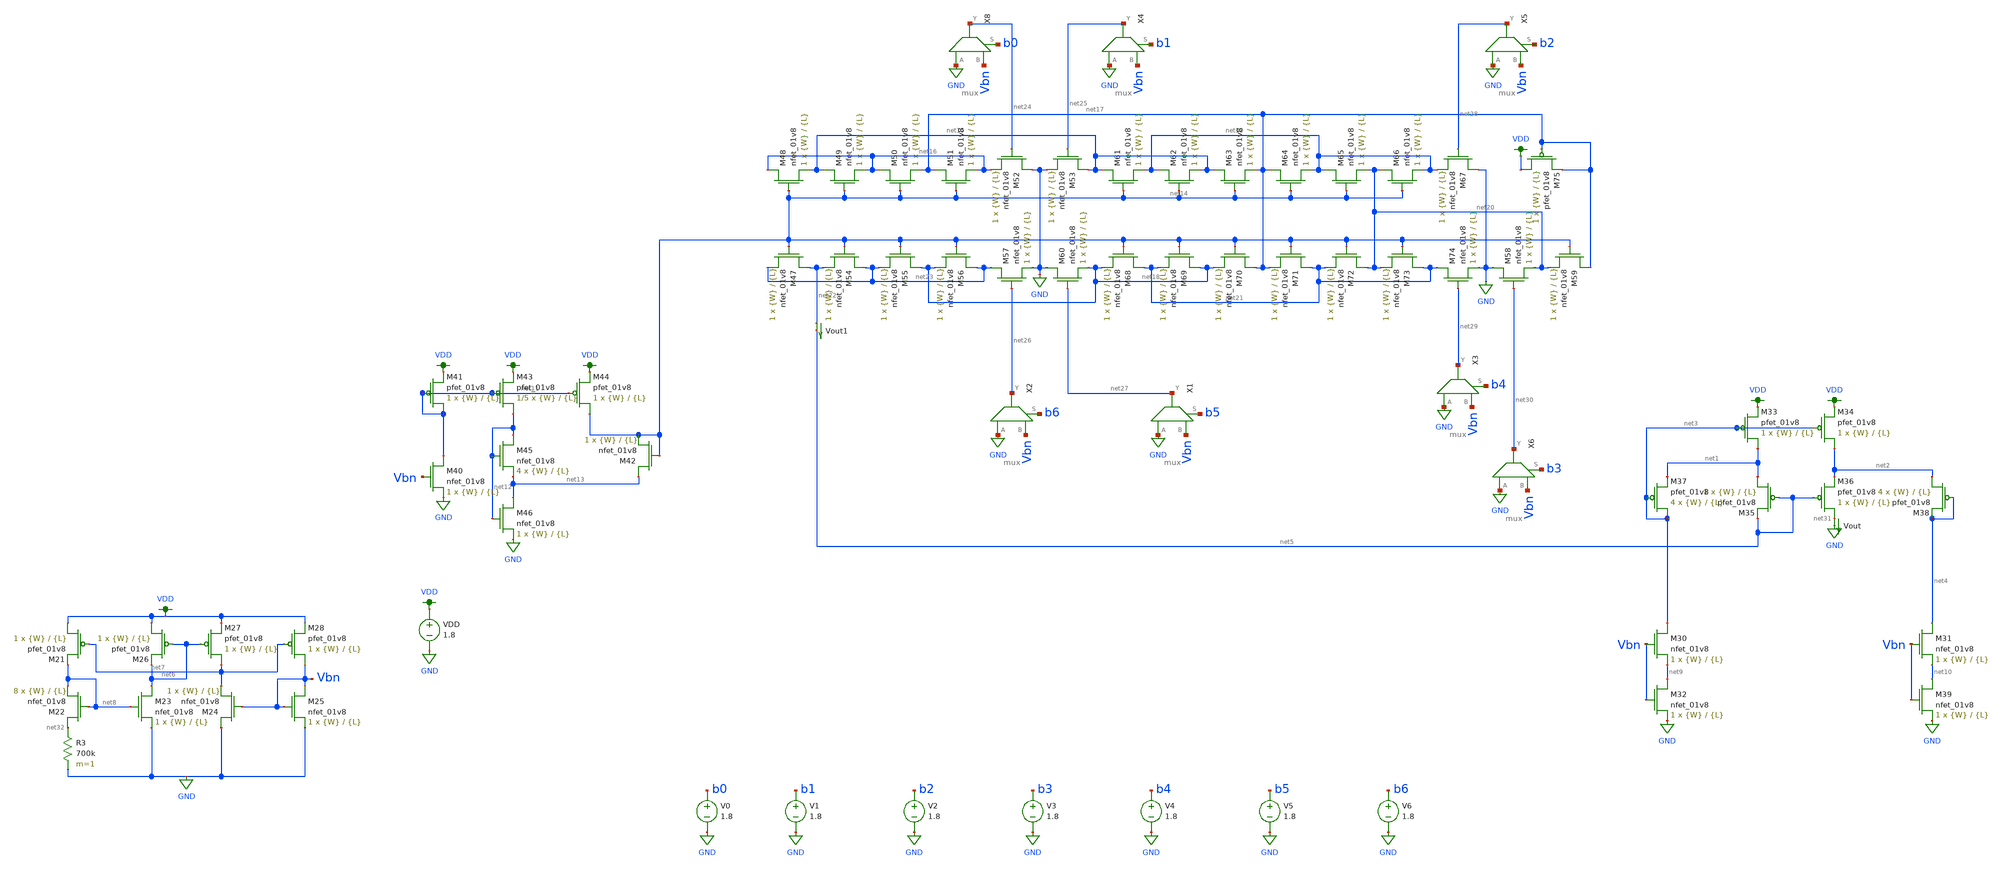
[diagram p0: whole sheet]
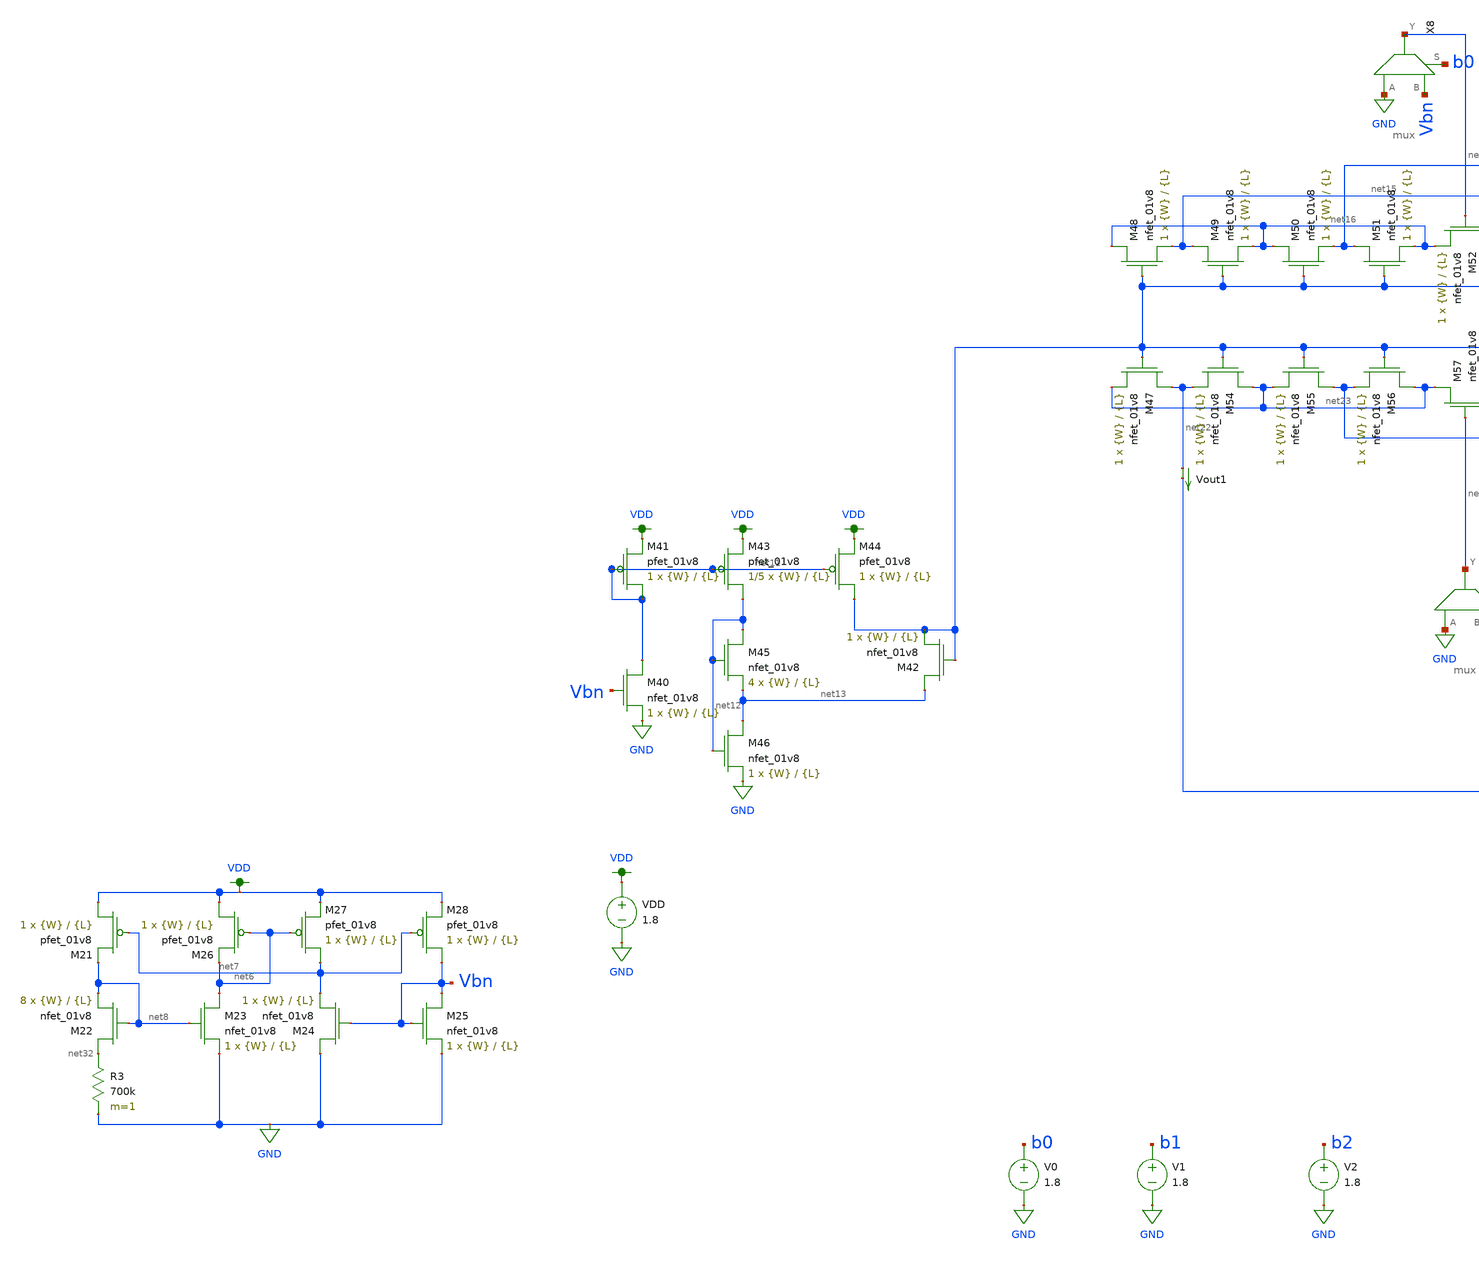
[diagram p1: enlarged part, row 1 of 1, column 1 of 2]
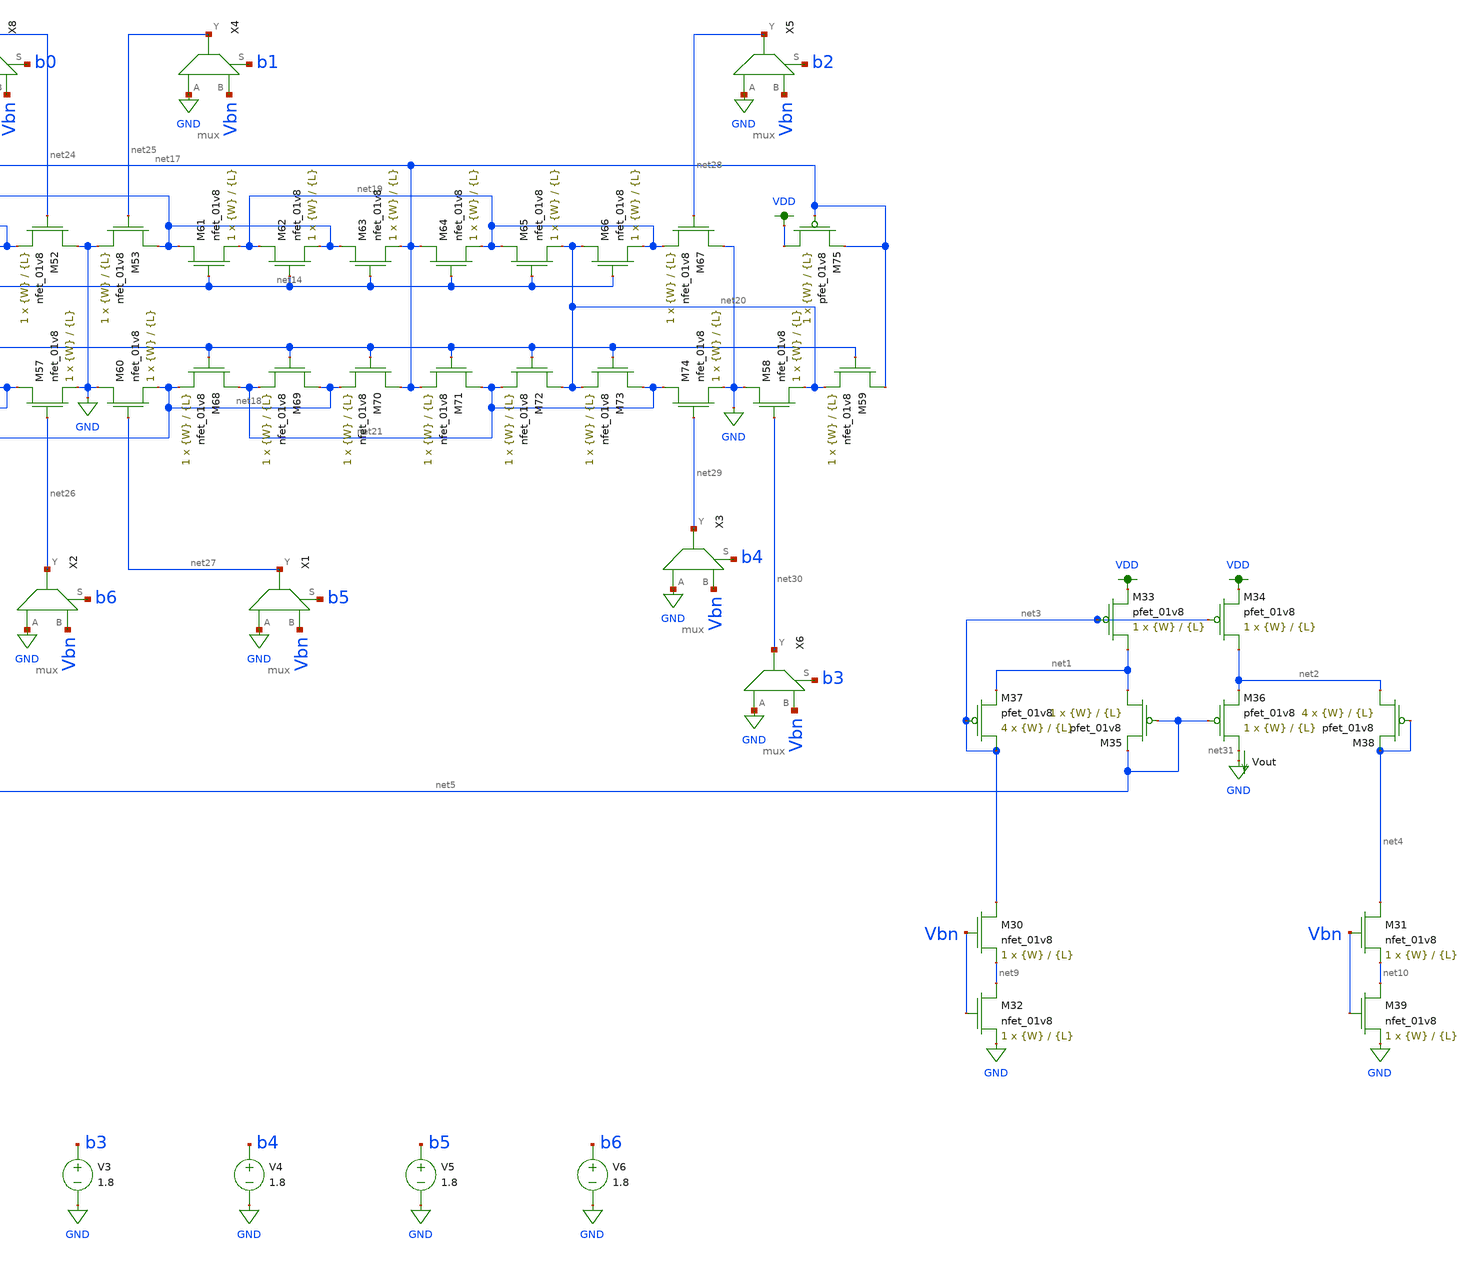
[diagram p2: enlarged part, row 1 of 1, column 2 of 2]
** sch_path: dac/schematics/misc/dac_lds_kenta.sch
**.subckt dac_lds_kenta
V0 b0 GND 1.8
V1 b1 GND 1.8
V2 b2 GND 1.8
V3 b3 GND 1.8
V4 b4 GND 1.8
V5 b5 GND 1.8
V6 b6 GND 1.8
Vout net31 GND 0
.save i(vout)
VDD VDD GND 1.8
XM33 net1 net3 VDD VDD sky130_fd_pr__pfet_01v8 L={L} W={W} nf=1 ad='int((nf+1)/2) * W/nf * 0.29' as='int((nf+2)/2) * W/nf * 0.29'
+ pd='2*int((nf+1)/2) * (W/nf + 0.29)' ps='2*int((nf+2)/2) * (W/nf + 0.29)' nrd='0.29 / W' nrs='0.29 / W'
+ sa=0 sb=0 sd=0 mult=1 m=1
XM34 net2 net3 VDD VDD sky130_fd_pr__pfet_01v8 L={L} W={W} nf=1 ad='int((nf+1)/2) * W/nf * 0.29' as='int((nf+2)/2) * W/nf * 0.29'
+ pd='2*int((nf+1)/2) * (W/nf + 0.29)' ps='2*int((nf+2)/2) * (W/nf + 0.29)' nrd='0.29 / W' nrs='0.29 / W'
+ sa=0 sb=0 sd=0 mult=1 m=1
XM35 net1 net5 net5 VDD sky130_fd_pr__pfet_01v8 L={L} W={W} nf=1 ad='int((nf+1)/2) * W/nf * 0.29' as='int((nf+2)/2) * W/nf * 0.29'
+ pd='2*int((nf+1)/2) * (W/nf + 0.29)' ps='2*int((nf+2)/2) * (W/nf + 0.29)' nrd='0.29 / W' nrs='0.29 / W'
+ sa=0 sb=0 sd=0 mult=1 m=1
XM36 net31 net5 net2 VDD sky130_fd_pr__pfet_01v8 L={L} W={W} nf=1 ad='int((nf+1)/2) * W/nf * 0.29' as='int((nf+2)/2) * W/nf * 0.29'
+ pd='2*int((nf+1)/2) * (W/nf + 0.29)' ps='2*int((nf+2)/2) * (W/nf + 0.29)' nrd='0.29 / W' nrs='0.29 / W'
+ sa=0 sb=0 sd=0 mult=1 m=1
XM37 net3 net3 net1 VDD sky130_fd_pr__pfet_01v8 L={L} W={W} nf=1 ad='int((nf+1)/2) * W/nf * 0.29' as='int((nf+2)/2) * W/nf * 0.29'
+ pd='2*int((nf+1)/2) * (W/nf + 0.29)' ps='2*int((nf+2)/2) * (W/nf + 0.29)' nrd='0.29 / W' nrs='0.29 / W'
+ sa=0 sb=0 sd=0 mult=4 m=4
XM38 net2 net4 net4 VDD sky130_fd_pr__pfet_01v8 L={L} W={W} nf=1 ad='int((nf+1)/2) * W/nf * 0.29' as='int((nf+2)/2) * W/nf * 0.29'
+ pd='2*int((nf+1)/2) * (W/nf + 0.29)' ps='2*int((nf+2)/2) * (W/nf + 0.29)' nrd='0.29 / W' nrs='0.29 / W'
+ sa=0 sb=0 sd=0 mult=4 m=4
XM21 VDD net7 net8 VDD sky130_fd_pr__pfet_01v8 L={L} W={W} nf=1 ad='int((nf+1)/2) * W/nf * 0.29' as='int((nf+2)/2) * W/nf * 0.29'
+ pd='2*int((nf+1)/2) * (W/nf + 0.29)' ps='2*int((nf+2)/2) * (W/nf + 0.29)' nrd='0.29 / W' nrs='0.29 / W'
+ sa=0 sb=0 sd=0 mult=1 m=1
XM22 net32 net8 net8 GND sky130_fd_pr__nfet_01v8 L={L} W={W} nf=1 ad='int((nf+1)/2) * W/nf * 0.29' as='int((nf+2)/2) * W/nf * 0.29'
+ pd='2*int((nf+1)/2) * (W/nf + 0.29)' ps='2*int((nf+2)/2) * (W/nf + 0.29)' nrd='0.29 / W' nrs='0.29 / W'
+ sa=0 sb=0 sd=0 mult=8 m=8
R3 net32 GND 700k m=1
XM23 net6 net8 GND GND sky130_fd_pr__nfet_01v8 L={L} W={W} nf=1 ad='int((nf+1)/2) * W/nf * 0.29' as='int((nf+2)/2) * W/nf * 0.29'
+ pd='2*int((nf+1)/2) * (W/nf + 0.29)' ps='2*int((nf+2)/2) * (W/nf + 0.29)' nrd='0.29 / W' nrs='0.29 / W'
+ sa=0 sb=0 sd=0 mult=1 m=1
XM24 GND Vbn net7 GND sky130_fd_pr__nfet_01v8 L={L} W={W} nf=1 ad='int((nf+1)/2) * W/nf * 0.29' as='int((nf+2)/2) * W/nf * 0.29'
+ pd='2*int((nf+1)/2) * (W/nf + 0.29)' ps='2*int((nf+2)/2) * (W/nf + 0.29)' nrd='0.29 / W' nrs='0.29 / W'
+ sa=0 sb=0 sd=0 mult=1 m=1
XM25 Vbn Vbn GND GND sky130_fd_pr__nfet_01v8 L={L} W={W} nf=1 ad='int((nf+1)/2) * W/nf * 0.29' as='int((nf+2)/2) * W/nf * 0.29'
+ pd='2*int((nf+1)/2) * (W/nf + 0.29)' ps='2*int((nf+2)/2) * (W/nf + 0.29)' nrd='0.29 / W' nrs='0.29 / W'
+ sa=0 sb=0 sd=0 mult=1 m=1
XM26 VDD net6 net6 VDD sky130_fd_pr__pfet_01v8 L={L} W={W} nf=1 ad='int((nf+1)/2) * W/nf * 0.29' as='int((nf+2)/2) * W/nf * 0.29'
+ pd='2*int((nf+1)/2) * (W/nf + 0.29)' ps='2*int((nf+2)/2) * (W/nf + 0.29)' nrd='0.29 / W' nrs='0.29 / W'
+ sa=0 sb=0 sd=0 mult=1 m=1
XM27 net7 net6 VDD VDD sky130_fd_pr__pfet_01v8 L={L} W={W} nf=1 ad='int((nf+1)/2) * W/nf * 0.29' as='int((nf+2)/2) * W/nf * 0.29'
+ pd='2*int((nf+1)/2) * (W/nf + 0.29)' ps='2*int((nf+2)/2) * (W/nf + 0.29)' nrd='0.29 / W' nrs='0.29 / W'
+ sa=0 sb=0 sd=0 mult=1 m=1
XM28 Vbn net7 VDD VDD sky130_fd_pr__pfet_01v8 L={L} W={W} nf=1 ad='int((nf+1)/2) * W/nf * 0.29' as='int((nf+2)/2) * W/nf * 0.29'
+ pd='2*int((nf+1)/2) * (W/nf + 0.29)' ps='2*int((nf+2)/2) * (W/nf + 0.29)' nrd='0.29 / W' nrs='0.29 / W'
+ sa=0 sb=0 sd=0 mult=1 m=1
XM30 net3 Vbn net9 GND sky130_fd_pr__nfet_01v8 L={L} W={W} nf=1 ad='int((nf+1)/2) * W/nf * 0.29' as='int((nf+2)/2) * W/nf * 0.29'
+ pd='2*int((nf+1)/2) * (W/nf + 0.29)' ps='2*int((nf+2)/2) * (W/nf + 0.29)' nrd='0.29 / W' nrs='0.29 / W'
+ sa=0 sb=0 sd=0 mult=1 m=1
XM31 net4 Vbn net10 GND sky130_fd_pr__nfet_01v8 L={L} W={W} nf=1 ad='int((nf+1)/2) * W/nf * 0.29' as='int((nf+2)/2) * W/nf * 0.29'
+ pd='2*int((nf+1)/2) * (W/nf + 0.29)' ps='2*int((nf+2)/2) * (W/nf + 0.29)' nrd='0.29 / W' nrs='0.29 / W'
+ sa=0 sb=0 sd=0 mult=1 m=1
XM32 net9 Vbn GND GND sky130_fd_pr__nfet_01v8 L={L} W={W} nf=1 ad='int((nf+1)/2) * W/nf * 0.29' as='int((nf+2)/2) * W/nf * 0.29'
+ pd='2*int((nf+1)/2) * (W/nf + 0.29)' ps='2*int((nf+2)/2) * (W/nf + 0.29)' nrd='0.29 / W' nrs='0.29 / W'
+ sa=0 sb=0 sd=0 mult=1 m=1
XM39 net10 Vbn GND GND sky130_fd_pr__nfet_01v8 L={L} W={W} nf=1 ad='int((nf+1)/2) * W/nf * 0.29' as='int((nf+2)/2) * W/nf * 0.29'
+ pd='2*int((nf+1)/2) * (W/nf + 0.29)' ps='2*int((nf+2)/2) * (W/nf + 0.29)' nrd='0.29 / W' nrs='0.29 / W'
+ sa=0 sb=0 sd=0 mult=1 m=1
X8 GND Vbn net24 b0 mux
X4 GND Vbn net25 b1 mux
X5 GND Vbn net28 b2 mux
X6 GND Vbn net30 b3 mux
X3 GND Vbn net29 b4 mux
X1 GND Vbn net27 b5 mux
X2 GND Vbn net26 b6 mux
Vout1 net22 net5 0
.save i(vout1)
XM40 net11 Vbn GND GND sky130_fd_pr__nfet_01v8 L={L} W={W} nf=1 ad='int((nf+1)/2) * W/nf * 0.29' as='int((nf+2)/2) * W/nf * 0.29'
+ pd='2*int((nf+1)/2) * (W/nf + 0.29)' ps='2*int((nf+2)/2) * (W/nf + 0.29)' nrd='0.29 / W' nrs='0.29 / W'
+ sa=0 sb=0 sd=0 mult=1 m=1
XM41 net11 net11 VDD VDD sky130_fd_pr__pfet_01v8 L={L} W={W} nf=1 ad='int((nf+1)/2) * W/nf * 0.29' as='int((nf+2)/2) * W/nf * 0.29'
+ pd='2*int((nf+1)/2) * (W/nf + 0.29)' ps='2*int((nf+2)/2) * (W/nf + 0.29)' nrd='0.29 / W' nrs='0.29 / W'
+ sa=0 sb=0 sd=0 mult=1 m=1
XM42 net13 net14 net14 GND sky130_fd_pr__nfet_01v8 L={L} W={W} nf=1 ad='int((nf+1)/2) * W/nf * 0.29'
+ as='int((nf+2)/2) * W/nf * 0.29' pd='2*int((nf+1)/2) * (W/nf + 0.29)' ps='2*int((nf+2)/2) * (W/nf + 0.29)'
+ nrd='0.29 / W' nrs='0.29 / W' sa=0 sb=0 sd=0 mult=1 m=1
XM43 net12 net11 VDD VDD sky130_fd_pr__pfet_01v8 L={L} W={W} nf=1 ad='int((nf+1)/2) * W/nf * 0.29' as='int((nf+2)/2) * W/nf * 0.29'
+ pd='2*int((nf+1)/2) * (W/nf + 0.29)' ps='2*int((nf+2)/2) * (W/nf + 0.29)' nrd='0.29 / W' nrs='0.29 / W'
+ sa=0 sb=0 sd=0 mult=1/5 m=1/5
XM44 net14 net11 VDD VDD sky130_fd_pr__pfet_01v8 L={L} W={W} nf=1 ad='int((nf+1)/2) * W/nf * 0.29' as='int((nf+2)/2) * W/nf * 0.29'
+ pd='2*int((nf+1)/2) * (W/nf + 0.29)' ps='2*int((nf+2)/2) * (W/nf + 0.29)' nrd='0.29 / W' nrs='0.29 / W'
+ sa=0 sb=0 sd=0 mult=1 m=1
XM45 net12 net12 net13 GND sky130_fd_pr__nfet_01v8 L={L} W={W} nf=1 ad='int((nf+1)/2) * W/nf * 0.29'
+ as='int((nf+2)/2) * W/nf * 0.29' pd='2*int((nf+1)/2) * (W/nf + 0.29)' ps='2*int((nf+2)/2) * (W/nf + 0.29)'
+ nrd='0.29 / W' nrs='0.29 / W' sa=0 sb=0 sd=0 mult=4 m=4
XM46 net13 net12 GND GND sky130_fd_pr__nfet_01v8 L={L} W={W} nf=1 ad='int((nf+1)/2) * W/nf * 0.29' as='int((nf+2)/2) * W/nf * 0.29'
+ pd='2*int((nf+1)/2) * (W/nf + 0.29)' ps='2*int((nf+2)/2) * (W/nf + 0.29)' nrd='0.29 / W' nrs='0.29 / W'
+ sa=0 sb=0 sd=0 mult=1 m=1
XM48 net16 net14 net15 GND sky130_fd_pr__nfet_01v8 L={L} W={W} nf=1 ad='int((nf+1)/2) * W/nf * 0.29'
+ as='int((nf+2)/2) * W/nf * 0.29' pd='2*int((nf+1)/2) * (W/nf + 0.29)' ps='2*int((nf+2)/2) * (W/nf + 0.29)'
+ nrd='0.29 / W' nrs='0.29 / W' sa=0 sb=0 sd=0 mult=1 m=1
XM49 net15 net14 net16 GND sky130_fd_pr__nfet_01v8 L={L} W={W} nf=1 ad='int((nf+1)/2) * W/nf * 0.29'
+ as='int((nf+2)/2) * W/nf * 0.29' pd='2*int((nf+1)/2) * (W/nf + 0.29)' ps='2*int((nf+2)/2) * (W/nf + 0.29)'
+ nrd='0.29 / W' nrs='0.29 / W' sa=0 sb=0 sd=0 mult=1 m=1
XM50 net16 net14 net17 GND sky130_fd_pr__nfet_01v8 L={L} W={W} nf=1 ad='int((nf+1)/2) * W/nf * 0.29'
+ as='int((nf+2)/2) * W/nf * 0.29' pd='2*int((nf+1)/2) * (W/nf + 0.29)' ps='2*int((nf+2)/2) * (W/nf + 0.29)'
+ nrd='0.29 / W' nrs='0.29 / W' sa=0 sb=0 sd=0 mult=1 m=1
XM51 net17 net14 net16 GND sky130_fd_pr__nfet_01v8 L={L} W={W} nf=1 ad='int((nf+1)/2) * W/nf * 0.29'
+ as='int((nf+2)/2) * W/nf * 0.29' pd='2*int((nf+1)/2) * (W/nf + 0.29)' ps='2*int((nf+2)/2) * (W/nf + 0.29)'
+ nrd='0.29 / W' nrs='0.29 / W' sa=0 sb=0 sd=0 mult=1 m=1
XM52 GND net24 net16 GND sky130_fd_pr__nfet_01v8 L={L} W={W} nf=1 ad='int((nf+1)/2) * W/nf * 0.29' as='int((nf+2)/2) * W/nf * 0.29'
+ pd='2*int((nf+1)/2) * (W/nf + 0.29)' ps='2*int((nf+2)/2) * (W/nf + 0.29)' nrd='0.29 / W' nrs='0.29 / W'
+ sa=0 sb=0 sd=0 mult=1 m=1
XM53 net15 net25 GND GND sky130_fd_pr__nfet_01v8 L={L} W={W} nf=1 ad='int((nf+1)/2) * W/nf * 0.29' as='int((nf+2)/2) * W/nf * 0.29'
+ pd='2*int((nf+1)/2) * (W/nf + 0.29)' ps='2*int((nf+2)/2) * (W/nf + 0.29)' nrd='0.29 / W' nrs='0.29 / W'
+ sa=0 sb=0 sd=0 mult=1 m=1
XM60 GND net27 net18 GND sky130_fd_pr__nfet_01v8 L={L} W={W} nf=1 ad='int((nf+1)/2) * W/nf * 0.29' as='int((nf+2)/2) * W/nf * 0.29'
+ pd='2*int((nf+1)/2) * (W/nf + 0.29)' ps='2*int((nf+2)/2) * (W/nf + 0.29)' nrd='0.29 / W' nrs='0.29 / W'
+ sa=0 sb=0 sd=0 mult=1 m=1
XM61 net15 net14 net19 GND sky130_fd_pr__nfet_01v8 L={L} W={W} nf=1 ad='int((nf+1)/2) * W/nf * 0.29'
+ as='int((nf+2)/2) * W/nf * 0.29' pd='2*int((nf+1)/2) * (W/nf + 0.29)' ps='2*int((nf+2)/2) * (W/nf + 0.29)'
+ nrd='0.29 / W' nrs='0.29 / W' sa=0 sb=0 sd=0 mult=1 m=1
XM62 net19 net14 net15 GND sky130_fd_pr__nfet_01v8 L={L} W={W} nf=1 ad='int((nf+1)/2) * W/nf * 0.29'
+ as='int((nf+2)/2) * W/nf * 0.29' pd='2*int((nf+1)/2) * (W/nf + 0.29)' ps='2*int((nf+2)/2) * (W/nf + 0.29)'
+ nrd='0.29 / W' nrs='0.29 / W' sa=0 sb=0 sd=0 mult=1 m=1
XM63 net15 net14 net17 GND sky130_fd_pr__nfet_01v8 L={L} W={W} nf=1 ad='int((nf+1)/2) * W/nf * 0.29'
+ as='int((nf+2)/2) * W/nf * 0.29' pd='2*int((nf+1)/2) * (W/nf + 0.29)' ps='2*int((nf+2)/2) * (W/nf + 0.29)'
+ nrd='0.29 / W' nrs='0.29 / W' sa=0 sb=0 sd=0 mult=1 m=1
XM64 net17 net14 net19 GND sky130_fd_pr__nfet_01v8 L={L} W={W} nf=1 ad='int((nf+1)/2) * W/nf * 0.29'
+ as='int((nf+2)/2) * W/nf * 0.29' pd='2*int((nf+1)/2) * (W/nf + 0.29)' ps='2*int((nf+2)/2) * (W/nf + 0.29)'
+ nrd='0.29 / W' nrs='0.29 / W' sa=0 sb=0 sd=0 mult=1 m=1
XM65 net19 net14 net20 GND sky130_fd_pr__nfet_01v8 L={L} W={W} nf=1 ad='int((nf+1)/2) * W/nf * 0.29'
+ as='int((nf+2)/2) * W/nf * 0.29' pd='2*int((nf+1)/2) * (W/nf + 0.29)' ps='2*int((nf+2)/2) * (W/nf + 0.29)'
+ nrd='0.29 / W' nrs='0.29 / W' sa=0 sb=0 sd=0 mult=1 m=1
XM66 net20 net14 net19 GND sky130_fd_pr__nfet_01v8 L={L} W={W} nf=1 ad='int((nf+1)/2) * W/nf * 0.29'
+ as='int((nf+2)/2) * W/nf * 0.29' pd='2*int((nf+1)/2) * (W/nf + 0.29)' ps='2*int((nf+2)/2) * (W/nf + 0.29)'
+ nrd='0.29 / W' nrs='0.29 / W' sa=0 sb=0 sd=0 mult=1 m=1
XM67 GND net28 net19 GND sky130_fd_pr__nfet_01v8 L={L} W={W} nf=1 ad='int((nf+1)/2) * W/nf * 0.29' as='int((nf+2)/2) * W/nf * 0.29'
+ pd='2*int((nf+1)/2) * (W/nf + 0.29)' ps='2*int((nf+2)/2) * (W/nf + 0.29)' nrd='0.29 / W' nrs='0.29 / W'
+ sa=0 sb=0 sd=0 mult=1 m=1
XM68 net21 net14 net18 GND sky130_fd_pr__nfet_01v8 L={L} W={W} nf=1 ad='int((nf+1)/2) * W/nf * 0.29'
+ as='int((nf+2)/2) * W/nf * 0.29' pd='2*int((nf+1)/2) * (W/nf + 0.29)' ps='2*int((nf+2)/2) * (W/nf + 0.29)'
+ nrd='0.29 / W' nrs='0.29 / W' sa=0 sb=0 sd=0 mult=1 m=1
XM69 net18 net14 net21 GND sky130_fd_pr__nfet_01v8 L={L} W={W} nf=1 ad='int((nf+1)/2) * W/nf * 0.29'
+ as='int((nf+2)/2) * W/nf * 0.29' pd='2*int((nf+1)/2) * (W/nf + 0.29)' ps='2*int((nf+2)/2) * (W/nf + 0.29)'
+ nrd='0.29 / W' nrs='0.29 / W' sa=0 sb=0 sd=0 mult=1 m=1
XM70 net17 net14 net18 GND sky130_fd_pr__nfet_01v8 L={L} W={W} nf=1 ad='int((nf+1)/2) * W/nf * 0.29'
+ as='int((nf+2)/2) * W/nf * 0.29' pd='2*int((nf+1)/2) * (W/nf + 0.29)' ps='2*int((nf+2)/2) * (W/nf + 0.29)'
+ nrd='0.29 / W' nrs='0.29 / W' sa=0 sb=0 sd=0 mult=1 m=1
XM71 net21 net14 net17 GND sky130_fd_pr__nfet_01v8 L={L} W={W} nf=1 ad='int((nf+1)/2) * W/nf * 0.29'
+ as='int((nf+2)/2) * W/nf * 0.29' pd='2*int((nf+1)/2) * (W/nf + 0.29)' ps='2*int((nf+2)/2) * (W/nf + 0.29)'
+ nrd='0.29 / W' nrs='0.29 / W' sa=0 sb=0 sd=0 mult=1 m=1
XM72 net20 net14 net21 GND sky130_fd_pr__nfet_01v8 L={L} W={W} nf=1 ad='int((nf+1)/2) * W/nf * 0.29'
+ as='int((nf+2)/2) * W/nf * 0.29' pd='2*int((nf+1)/2) * (W/nf + 0.29)' ps='2*int((nf+2)/2) * (W/nf + 0.29)'
+ nrd='0.29 / W' nrs='0.29 / W' sa=0 sb=0 sd=0 mult=1 m=1
XM73 net21 net14 net20 GND sky130_fd_pr__nfet_01v8 L={L} W={W} nf=1 ad='int((nf+1)/2) * W/nf * 0.29'
+ as='int((nf+2)/2) * W/nf * 0.29' pd='2*int((nf+1)/2) * (W/nf + 0.29)' ps='2*int((nf+2)/2) * (W/nf + 0.29)'
+ nrd='0.29 / W' nrs='0.29 / W' sa=0 sb=0 sd=0 mult=1 m=1
XM74 net21 net29 GND GND sky130_fd_pr__nfet_01v8 L={L} W={W} nf=1 ad='int((nf+1)/2) * W/nf * 0.29' as='int((nf+2)/2) * W/nf * 0.29'
+ pd='2*int((nf+1)/2) * (W/nf + 0.29)' ps='2*int((nf+2)/2) * (W/nf + 0.29)' nrd='0.29 / W' nrs='0.29 / W'
+ sa=0 sb=0 sd=0 mult=1 m=1
XM47 net22 net14 net23 GND sky130_fd_pr__nfet_01v8 L={L} W={W} nf=1 ad='int((nf+1)/2) * W/nf * 0.29'
+ as='int((nf+2)/2) * W/nf * 0.29' pd='2*int((nf+1)/2) * (W/nf + 0.29)' ps='2*int((nf+2)/2) * (W/nf + 0.29)'
+ nrd='0.29 / W' nrs='0.29 / W' sa=0 sb=0 sd=0 mult=1 m=1
XM54 net23 net14 net22 GND sky130_fd_pr__nfet_01v8 L={L} W={W} nf=1 ad='int((nf+1)/2) * W/nf * 0.29'
+ as='int((nf+2)/2) * W/nf * 0.29' pd='2*int((nf+1)/2) * (W/nf + 0.29)' ps='2*int((nf+2)/2) * (W/nf + 0.29)'
+ nrd='0.29 / W' nrs='0.29 / W' sa=0 sb=0 sd=0 mult=1 m=1
XM55 net18 net14 net23 GND sky130_fd_pr__nfet_01v8 L={L} W={W} nf=1 ad='int((nf+1)/2) * W/nf * 0.29'
+ as='int((nf+2)/2) * W/nf * 0.29' pd='2*int((nf+1)/2) * (W/nf + 0.29)' ps='2*int((nf+2)/2) * (W/nf + 0.29)'
+ nrd='0.29 / W' nrs='0.29 / W' sa=0 sb=0 sd=0 mult=1 m=1
XM56 net23 net14 net18 GND sky130_fd_pr__nfet_01v8 L={L} W={W} nf=1 ad='int((nf+1)/2) * W/nf * 0.29'
+ as='int((nf+2)/2) * W/nf * 0.29' pd='2*int((nf+1)/2) * (W/nf + 0.29)' ps='2*int((nf+2)/2) * (W/nf + 0.29)'
+ nrd='0.29 / W' nrs='0.29 / W' sa=0 sb=0 sd=0 mult=1 m=1
XM57 net23 net26 GND GND sky130_fd_pr__nfet_01v8 L={L} W={W} nf=1 ad='int((nf+1)/2) * W/nf * 0.29' as='int((nf+2)/2) * W/nf * 0.29'
+ pd='2*int((nf+1)/2) * (W/nf + 0.29)' ps='2*int((nf+2)/2) * (W/nf + 0.29)' nrd='0.29 / W' nrs='0.29 / W'
+ sa=0 sb=0 sd=0 mult=1 m=1
XM58 GND net30 net20 GND sky130_fd_pr__nfet_01v8 L={L} W={W} nf=1 ad='int((nf+1)/2) * W/nf * 0.29' as='int((nf+2)/2) * W/nf * 0.29'
+ pd='2*int((nf+1)/2) * (W/nf + 0.29)' ps='2*int((nf+2)/2) * (W/nf + 0.29)' nrd='0.29 / W' nrs='0.29 / W'
+ sa=0 sb=0 sd=0 mult=1 m=1
XM59 net17 net14 net20 GND sky130_fd_pr__nfet_01v8 L={L} W={W} nf=1 ad='int((nf+1)/2) * W/nf * 0.29'
+ as='int((nf+2)/2) * W/nf * 0.29' pd='2*int((nf+1)/2) * (W/nf + 0.29)' ps='2*int((nf+2)/2) * (W/nf + 0.29)'
+ nrd='0.29 / W' nrs='0.29 / W' sa=0 sb=0 sd=0 mult=1 m=1
XM75 VDD net17 net17 VDD sky130_fd_pr__pfet_01v8 L={L} W={W} nf=1 ad='int((nf+1)/2) * W/nf * 0.29' as='int((nf+2)/2) * W/nf * 0.29'
+ pd='2*int((nf+1)/2) * (W/nf + 0.29)' ps='2*int((nf+2)/2) * (W/nf + 0.29)' nrd='0.29 / W' nrs='0.29 / W'
+ sa=0 sb=0 sd=0 mult=1 m=1
**** begin user architecture code

.param W=24
.param L=1
.control
set wr_vecnames
set wr_singlescale
let code = 0
  while code < 128
    if code eq 0
      let b0 = 0
    else
      let b0 = code % 2 * 1.8
    end
    if floor(code / 2) eq 0
      let b1 = 0
    else
      let b1 = floor(code / 2) % 2 * 1.8
    end
    if floor(code / 4) eq 0
      let b2 = 0
    else
      let b2 = floor(code / 4) % 2 * 1.8
    end
    if floor(code / 8) eq 0
      let b3 = 0
    else
      let b3 = floor(code / 8) % 2 * 1.8
    end
    if floor(code / 16) eq 0
      let b4 = 0
    else
      let b4 = floor(code / 16) % 2 * 1.8
    end
    if floor(code / 32) eq 0
      let b5 = 0
    else
      let b5 = floor(code / 32) % 2 * 1.8
    end
    if floor(code / 64) eq 0
      let b6 = 0
    else
      let b6 = floor(code / 64) % 2 * 1.8
    end
    alter v0 $&b0
    alter v1 $&b1
    alter v2 $&b2
    alter v3 $&b3
    alter v4 $&b4
    alter v5 $&b5
    alter v6 $&b6
    save all
    op
    wrdata ~/Documents/current-output-dac-vlsi/simulations/dac_sim.txt v(Vbn) i(Vout) i(Vout1) v(b6)
+ v(b5) v(b4) v(b3) v(b2) v(b1) v(b0)
    if code eq 0
      set appendwrite
      set wr_vecnames = FALSE
    end
    let code = code + 1
  end
  quit
.endc


.option wnflag=1
.param MC_SWITCH=1.0
.lib ~/skywater/skywater-pdk/libraries/sky130_fd_pr_ngspice/latest/models/sky130.lib.spice tt

**** end user architecture code
**.ends

* expanding   symbol:  /home/madvlsi/Documents/current-output-dac-vlsi/schematics/mux.sym # of
*+ pins=4
** sym_path: dac/schematics/mux.sym
** sch_path: dac/schematics/mux.sch
.subckt mux A B Y S
*.ipin A
*.ipin B
*.ipin S
*.opin Y
XM1 A S Y VDD sky130_fd_pr__pfet_01v8 L=0.15 W=1 nf=1 ad='int((nf+1)/2) * W/nf * 0.29' as='int((nf+2)/2) * W/nf * 0.29'
+ pd='2*int((nf+1)/2) * (W/nf + 0.29)' ps='2*int((nf+2)/2) * (W/nf + 0.29)' nrd='0.29 / W' nrs='0.29 / W'
+ sa=0 sb=0 sd=0 mult=1 m=1
XM3 net1 S VDD VDD sky130_fd_pr__pfet_01v8 L=0.15 W=1 nf=1 ad='int((nf+1)/2) * W/nf * 0.29' as='int((nf+2)/2) * W/nf * 0.29'
+ pd='2*int((nf+1)/2) * (W/nf + 0.29)' ps='2*int((nf+2)/2) * (W/nf + 0.29)' nrd='0.29 / W' nrs='0.29 / W'
+ sa=0 sb=0 sd=0 mult=1 m=1
XM4 net1 S GND GND sky130_fd_pr__nfet_01v8 L=0.15 W=1 nf=1 ad='int((nf+1)/2) * W/nf * 0.29' as='int((nf+2)/2) * W/nf * 0.29'
+ pd='2*int((nf+1)/2) * (W/nf + 0.29)' ps='2*int((nf+2)/2) * (W/nf + 0.29)' nrd='0.29 / W' nrs='0.29 / W'
+ sa=0 sb=0 sd=0 mult=1 m=1
XM5 A net1 Y GND sky130_fd_pr__nfet_01v8 L=0.15 W=1 nf=1 ad='int((nf+1)/2) * W/nf * 0.29' as='int((nf+2)/2) * W/nf * 0.29'
+ pd='2*int((nf+1)/2) * (W/nf + 0.29)' ps='2*int((nf+2)/2) * (W/nf + 0.29)' nrd='0.29 / W' nrs='0.29 / W'
+ sa=0 sb=0 sd=0 mult=1 m=1
XM2 B net1 Y VDD sky130_fd_pr__pfet_01v8 L=0.15 W=1 nf=1 ad='int((nf+1)/2) * W/nf * 0.29' as='int((nf+2)/2) * W/nf * 0.29'
+ pd='2*int((nf+1)/2) * (W/nf + 0.29)' ps='2*int((nf+2)/2) * (W/nf + 0.29)' nrd='0.29 / W' nrs='0.29 / W'
+ sa=0 sb=0 sd=0 mult=1 m=1
XM6 B S Y GND sky130_fd_pr__nfet_01v8 L=0.15 W=1 nf=1 ad='int((nf+1)/2) * W/nf * 0.29' as='int((nf+2)/2) * W/nf * 0.29'
+ pd='2*int((nf+1)/2) * (W/nf + 0.29)' ps='2*int((nf+2)/2) * (W/nf + 0.29)' nrd='0.29 / W' nrs='0.29 / W'
+ sa=0 sb=0 sd=0 mult=1 m=1
.ends

.GLOBAL GND
.GLOBAL VDD
.end
